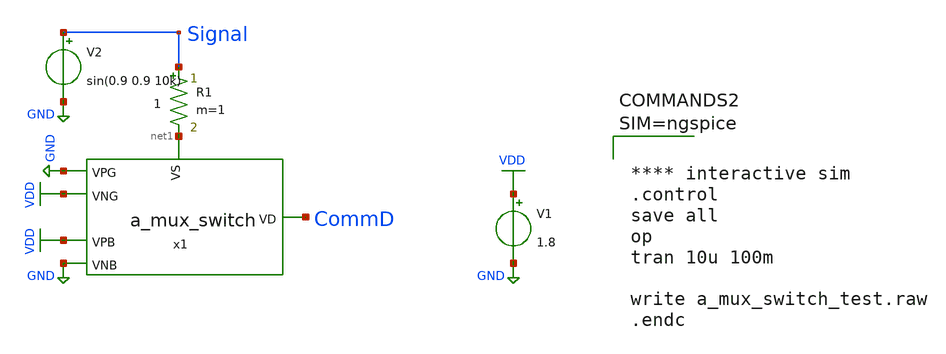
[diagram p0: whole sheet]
** sch_path: compiled 2/a_mux_switch_test.sch
**.subckt a_mux_switch_test
x1 GND VDD VDD GND net1 CommD a_mux_switch
V1 VDD GND 1.8
V2 Signal GND sin(0.9 0.9 10k)
R1 Signal net1 1 m=1
**** begin user architecture code

** opencircuitdesign pdks install
.lib $::SKYWATER_MODELS/sky130.lib.spice tt
.include $::SKYWATER_STDCELLS/sky130_fd_sc_hd.spice





**** interactive sim
.control
save all
op
tran 10u 100m

write a_mux_switch_test.raw
.endc



**** end user architecture code
**.ends

* expanding   symbol:  a_mux_switch.sym # of pins=6
** sym_path: analog_mux_files 2/a_mux_switch.sym
** sch_path: analog_mux_files 2/a_mux_switch.sch
.subckt a_mux_switch VNB VNG VPB VPG VS VD
*.ipin VPG
*.ipin VNG
*.ipin VS
*.opin VD
*.ipin VPB
*.ipin VNB
XM1 VD VPG VS VPB sky130_fd_pr__pfet_01v8 L=0.15 W=20 nf=1 ad='int((nf+1)/2) * W/nf * 0.29' as='int((nf+2)/2) * W/nf * 0.29'
+ pd='2*int((nf+1)/2) * (W/nf + 0.29)' ps='2*int((nf+2)/2) * (W/nf + 0.29)' nrd='0.29 / W' nrs='0.29 / W'
+ sa=0 sb=0 sd=0 mult=1 m=1
XM2 VD VNG VS VNB sky130_fd_pr__nfet_01v8 L=0.15 W=20 nf=1 ad='int((nf+1)/2) * W/nf * 0.29' as='int((nf+2)/2) * W/nf * 0.29'
+ pd='2*int((nf+1)/2) * (W/nf + 0.29)' ps='2*int((nf+2)/2) * (W/nf + 0.29)' nrd='0.29 / W' nrs='0.29 / W'
+ sa=0 sb=0 sd=0 mult=1 m=1
.ends

.GLOBAL GND
.GLOBAL VDD
.end
